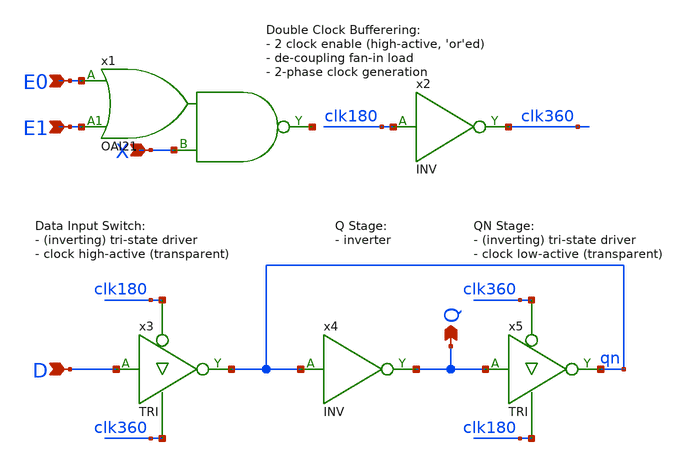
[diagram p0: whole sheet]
** sch_path: Sources/crafted/LATPEE.sch
**.subckt LATPEE X D Q E0 E1
*.ipin X
*.ipin D
*.opin Q
*.ipin E0
*.ipin E1
x1 E0 E1 X net1 VDD GND OAI21 Wmin=1.5u Lmin=1u g=2 m=1
x2 clk180 clk360 VDD GND INV Wmin=1.5u Lmin=1u g=2 m=1
x3 D clk180 clk360 qn VDD GND TRI Wmin=1.5u Lmin=1u g=2 m=1
x5 Q clk360 clk180 qn VDD GND TRI Wmin=1.5u Lmin=1u g=2 m=1
x4 qn Q VDD GND INV Wmin=1.5u Lmin=1u g=2 m=1
**.ends
.end
